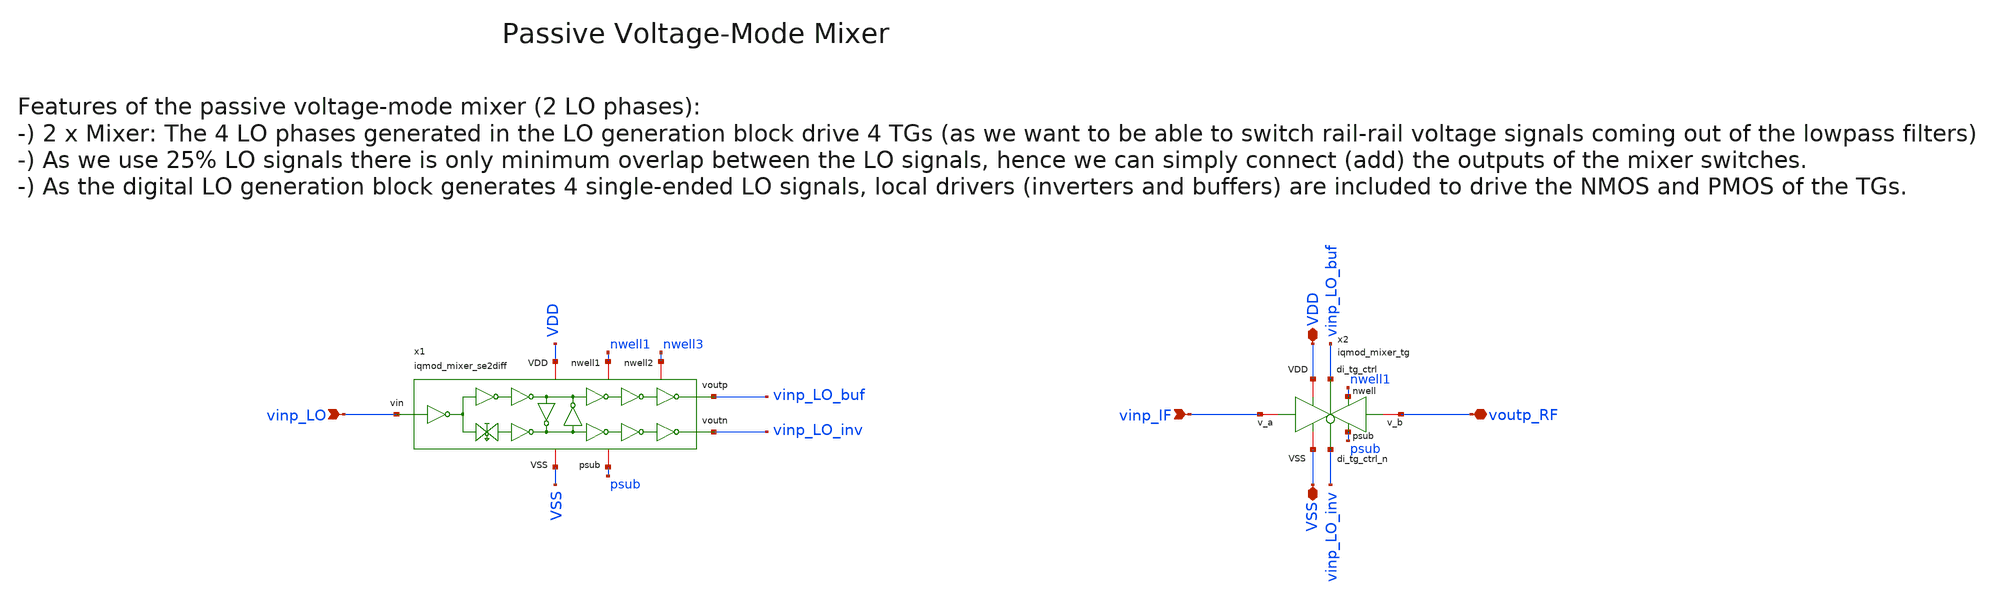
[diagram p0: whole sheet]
** sch_path: ihp130/macros/iqmod/xschem/iqmod_mixer_half.sch
**.subckt iqmod_mixer_half VDD VSS vinp_IF voutp_RF vinp_LO
*.iopin VDD
*.iopin VSS
*.ipin vinp_IF
*.iopin voutp_RF
*.ipin vinp_LO
x2 nwell1 psub VDD vinp_LO_buf VSS voutp_RF vinp_IF vinp_LO_inv iqmod_mixer_tg
x1 nwell1 psub nwell3 VDD vinp_LO vinp_LO_buf VSS vinp_LO_inv iqmod_mixer_se2diff
**.ends
.end
